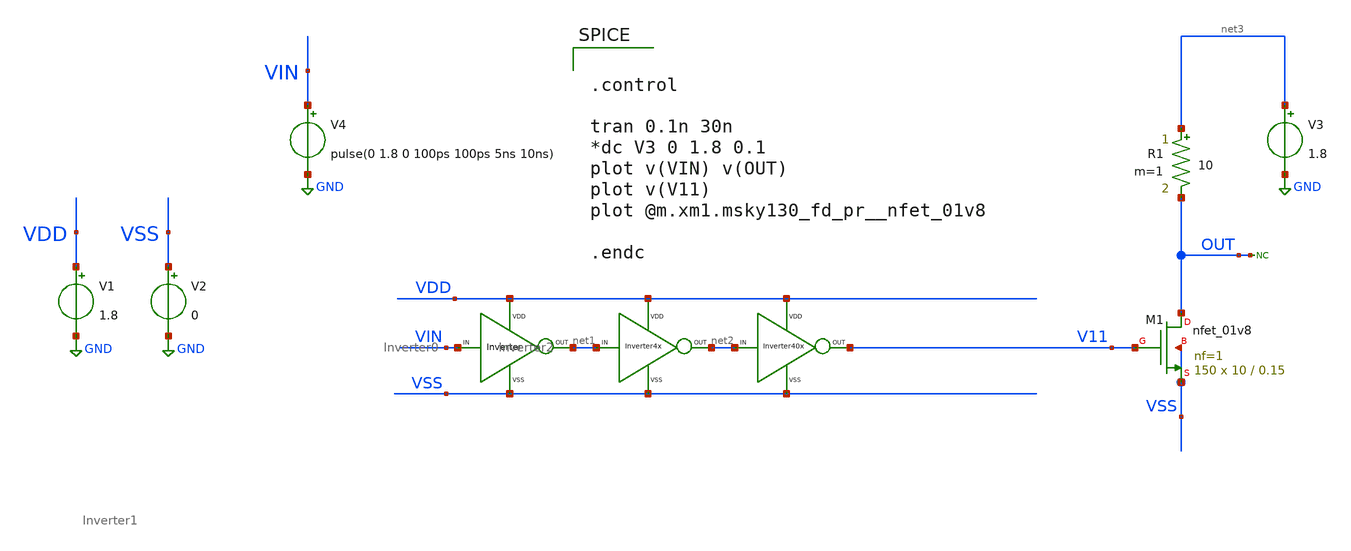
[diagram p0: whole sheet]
** sch_path: xschem/DC_DC_Converter_xschem/OTHERS/DC_DC_Converter_5/BUFFER/test_nmos.sch
**.subckt test_nmos
X7 VIN net1 VDD VSS Inverter0
X8 net1 net2 VDD VSS Inverter1
XM1 OUT V11 VSS VSS sky130_fd_pr__nfet_01v8 L=0.15 W=10 nf=1 ad='int((nf+1)/2) * W/nf * 0.29' as='int((nf+2)/2) * W/nf * 0.29'
+ pd='2*int((nf+1)/2) * (W/nf + 0.29)' ps='2*int((nf+2)/2) * (W/nf + 0.29)' nrd='0.29 / W' nrs='0.29 / W'
+ sa=0 sb=0 sd=0 mult=150 m=150
V1 VDD GND 1.8
V2 VSS GND 0
* noconn OUT
V4 VIN GND pulse(0 1.8 0 100ps 100ps 5ns 10ns)
V3 net3 GND 1.8
X1 net2 V11 VDD VSS Inverter2
R1 net3 OUT 10 m=1
**** begin user architecture code

** opencircuitdesign pdks install
.lib $::SKYWATER_MODELS/sky130.lib.spice tt




.control

tran 0.1n 30n
*dc V3 0 1.8 0.1
plot v(VIN) v(OUT)
plot v(V11)
plot @m.xm1.msky130_fd_pr__nfet_01v8

.endc


**** end user architecture code
**.ends
.GLOBAL GND
.end
